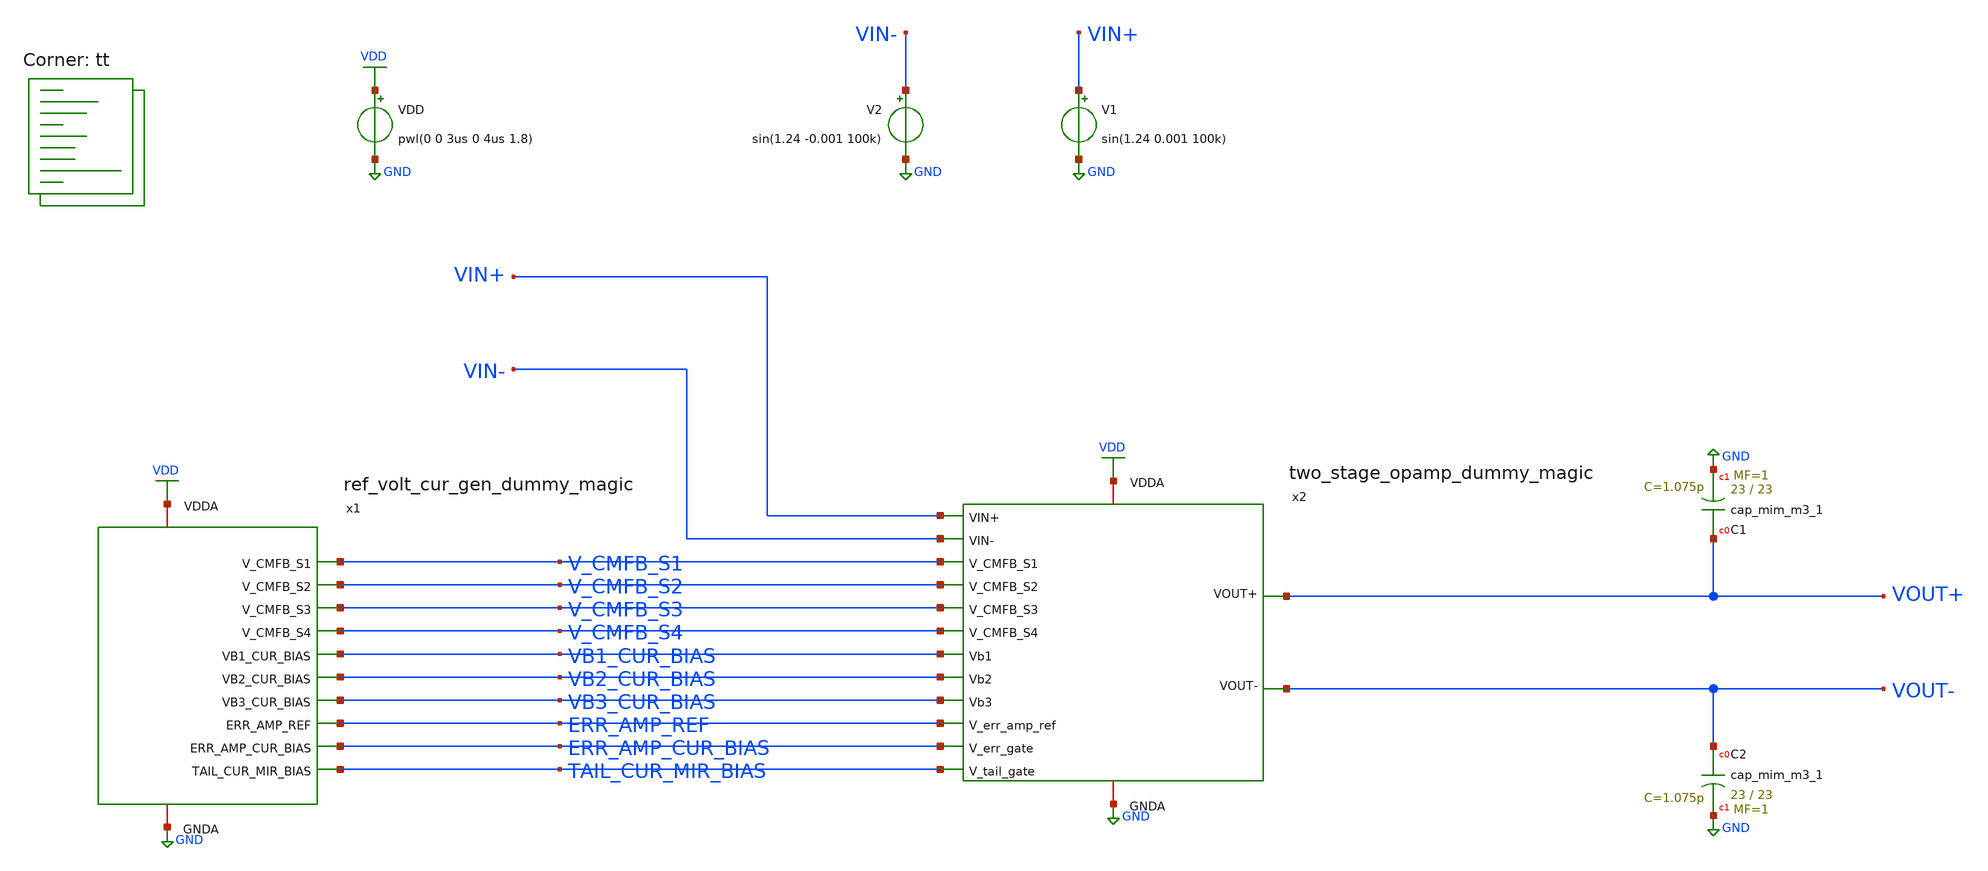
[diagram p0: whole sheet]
** sch_path: projects/opamp/xschem_ngspice/tb_two_stage_opamp_dummy_magic.sch
**.subckt tb_two_stage_opamp_dummy_magic
VDD VDD GND pwl(0 0 3us 0 4us 1.8)
V2 VIN- GND sin(1.24 -0.001 100k)
V1 VIN+ GND sin(1.24 0.001 100k)
XC1 VOUT+ GND sky130_fd_pr__cap_mim_m3_1 W=23 L=23 MF=1 m=1
XC2 VOUT- GND sky130_fd_pr__cap_mim_m3_1 W=23 L=23 MF=1 m=1
x1 VDD ERR_AMP_REF V_CMFB_S3 VB1_CUR_BIAS TAIL_CUR_MIR_BIAS V_CMFB_S1 ERR_AMP_CUR_BIAS VB3_CUR_BIAS
+ V_CMFB_S4 V_CMFB_S2 VB2_CUR_BIAS GND ref_volt_cur_gen_dummy_magic
x2 VDD V_CMFB_S1 V_CMFB_S3 VB3_CUR_BIAS VB2_CUR_BIAS VB1_CUR_BIAS V_CMFB_S2 V_CMFB_S4 VOUT- VOUT+
+ TAIL_CUR_MIR_BIAS ERR_AMP_REF ERR_AMP_CUR_BIAS VIN+ VIN- GND two_stage_opamp_dummy_magic
**** begin user architecture code
.lib $::SKYWATER_MODELS/sky130.lib.spice tt




.include /foss/designs/my_design/projects/opamp/xschem_ngspice/ref_volt_cur_gen_dummy_magic.spice
.include /foss/designs/my_design/projects/opamp/xschem_ngspice/two_stage_opamp_dummy_magic.spice

.include /foss/designs/my_design/projects/bandgapref/xschem_ngspice/new_files/low_voltage_BGR_dummy_magic.spice

.option method=gear
.option wnflag=1
.option savecurrents

.save @m.x1.xm1.msky130_fd_pr__pfet_01v8[gm] @m.x1.xm1.msky130_fd_pr__pfet_01v8[vth] @m.x1.xm2.msky130_fd_pr__pfet_01v8[gm] @m.x1.xm2.msky130_fd_pr__pfet_01v8[vth] @m.x1.xm3.msky130_fd_pr__pfet_01v8[gm] @m.x1.xm3.msky130_fd_pr__pfet_01v8[vth] @m.x1.xm4.msky130_fd_pr__pfet_01v8[gm] @m.x1.xm4.msky130_fd_pr__pfet_01v8[vth] @m.x1.xm5.msky130_fd_pr__nfet_01v8[gm] @m.x1.xm5.msky130_fd_pr__nfet_01v8[vth] @m.x1.xm6.msky130_fd_pr__pfet_01v8[gm] @m.x1.xm6.msky130_fd_pr__pfet_01v8[vth] @m.x1.xm7.msky130_fd_pr__nfet_01v8[gm] @m.x1.xm7.msky130_fd_pr__nfet_01v8[vth] @m.x1.xm8.msky130_fd_pr__pfet_01v8[gm] @m.x1.xm8.msky130_fd_pr__pfet_01v8[vth] @m.x2.xm2.msky130_fd_pr__nfet_01v8[gm] @m.x2.xm2.msky130_fd_pr__nfet_01v8[vth] @m.x2.xm3.msky130_fd_pr__nfet_01v8[gm] @m.x2.xm3.msky130_fd_pr__nfet_01v8[vth] @m.x2.xm7.msky130_fd_pr__pfet_01v8[gm] @m.x2.xm7.msky130_fd_pr__pfet_01v8[vth] @m.x1.x1.xm1.msky130_fd_pr__nfet_01v8[gm] @m.x1.x1.xm2.msky130_fd_pr__nfet_01v8[gm] @m.x1.x1.xm3.msky130_fd_pr__nfet_01v8[gm] @m.x1.x1.xm4.msky130_fd_pr__nfet_01v8[gm] @m.x1.x1.xm5.msky130_fd_pr__pfet_01v8[gm] @m.x1.x1.xm6.msky130_fd_pr__nfet_01v8[gm] @m.x1.x1.xm7.msky130_fd_pr__pfet_01v8[gm] @m.x1.x2.xm1.msky130_fd_pr__nfet_01v8[gm] @m.x1.x2.xm2.msky130_fd_pr__nfet_01v8[gm] @m.x1.x2.xm3.msky130_fd_pr__nfet_01v8[gm] @m.x1.x2.xm4.msky130_fd_pr__nfet_01v8[gm] @m.x1.x2.xm5.msky130_fd_pr__pfet_01v8[gm] @m.x1.x2.xm6.msky130_fd_pr__nfet_01v8[gm] @m.x1.x2.xm7.msky130_fd_pr__pfet_01v8[gm] @m.x2.xm39.msky130_fd_pr__pfet_01v8[gm] @m.x2.xm39.msky130_fd_pr__pfet_01v8[vth] @m.x2.xm40.msky130_fd_pr__pfet_01v8[gm] @m.x2.xm40.msky130_fd_pr__pfet_01v8[vth]

* .ic v(v_top) = 1.8

.control

  * let runs=3
  * let run=1

  * dowhile run <= runs
    save v(vout+) v(vout-) v(vin+) v(vin-) v(x2.x) v(x2.y) v(x2.vb1) v(x2.vb2) v(x2.vb3) v(x2.v_tot)
    * save all
    remzerovec
    set appendwrite
    * dc temp -40 120 10 VDD 0 4.0 0.2
    * dc VDD 0 2.0 0.02 temp -40 120 40
    * dc V5 0 0.01 0.0001
    tran 2n 30u
    * tran 1p 3n
    * tran 0.1ns 30us
    * ac dec 40 1 10T
    write tb_two_stage_opamp_dummy_magic.raw
    * write tb_two_stage_opamp_dummy_magic_mc.raw
    * write tb_two_stage_opamp_dummy_magic_tt_mm.raw
    * write tb_two_stage_opamp_dummy_magic_AC.raw
    * reset
    * let run = run + 1
  * end
.endc




**** end user architecture code
**.ends
.GLOBAL GND
.GLOBAL VDD
.end
